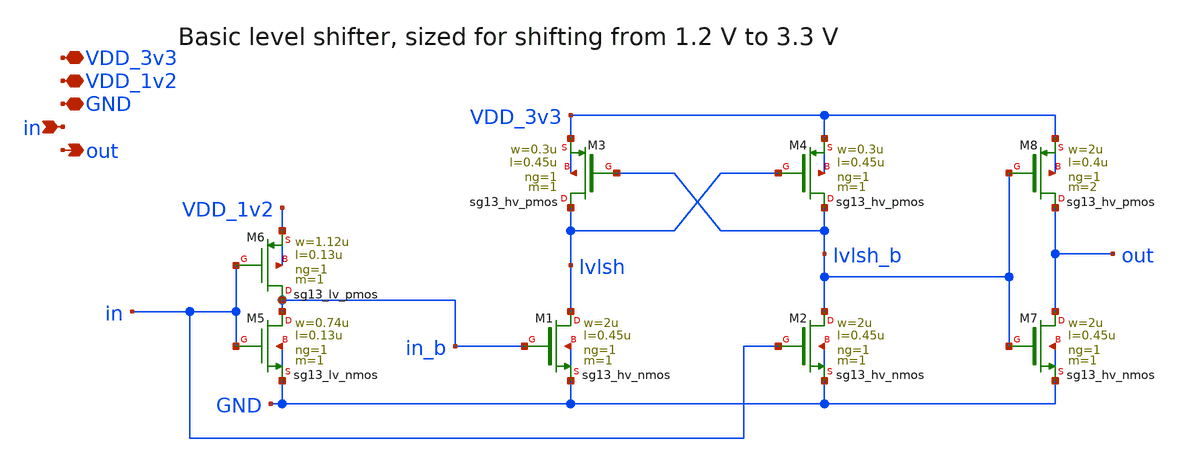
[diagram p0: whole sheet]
** sch_path: FLDO/design_data/xschem/shifter.sch
**.subckt shifter VDD_3v3 VDD_1v2 GND in out
*.iopin VDD_3v3
*.iopin VDD_1v2
*.iopin GND
*.ipin in
*.opin out
XM1 lvlsh in_b GND GND sg13_hv_nmos w=2u l=0.45u ng=1 m=1 mm_ok=1
XM2 lvlsh_b in GND GND sg13_hv_nmos w=2u l=0.45u ng=1 m=1 mm_ok=1
XM3 lvlsh lvlsh_b VDD_3v3 VDD_3v3 sg13_hv_pmos w=0.3u l=0.45u ng=1 m=1 mm_ok=1
XM4 lvlsh_b lvlsh VDD_3v3 VDD_3v3 sg13_hv_pmos w=0.3u l=0.45u ng=1 m=1 mm_ok=1
XM5 in_b in GND GND sg13_lv_nmos w=0.74u l=0.13u ng=1 m=1 mm_ok=1
XM6 in_b in VDD_1v2 VDD_1v2 sg13_lv_pmos w=1.12u l=0.13u ng=1 m=1 mm_ok=1
XM7 out lvlsh_b GND GND sg13_hv_nmos w=2u l=0.45u ng=1 m=1 mm_ok=1
XM8 out lvlsh_b VDD_3v3 VDD_3v3 sg13_hv_pmos w=2u l=0.4u ng=1 m=2 mm_ok=1
**.ends
.end
